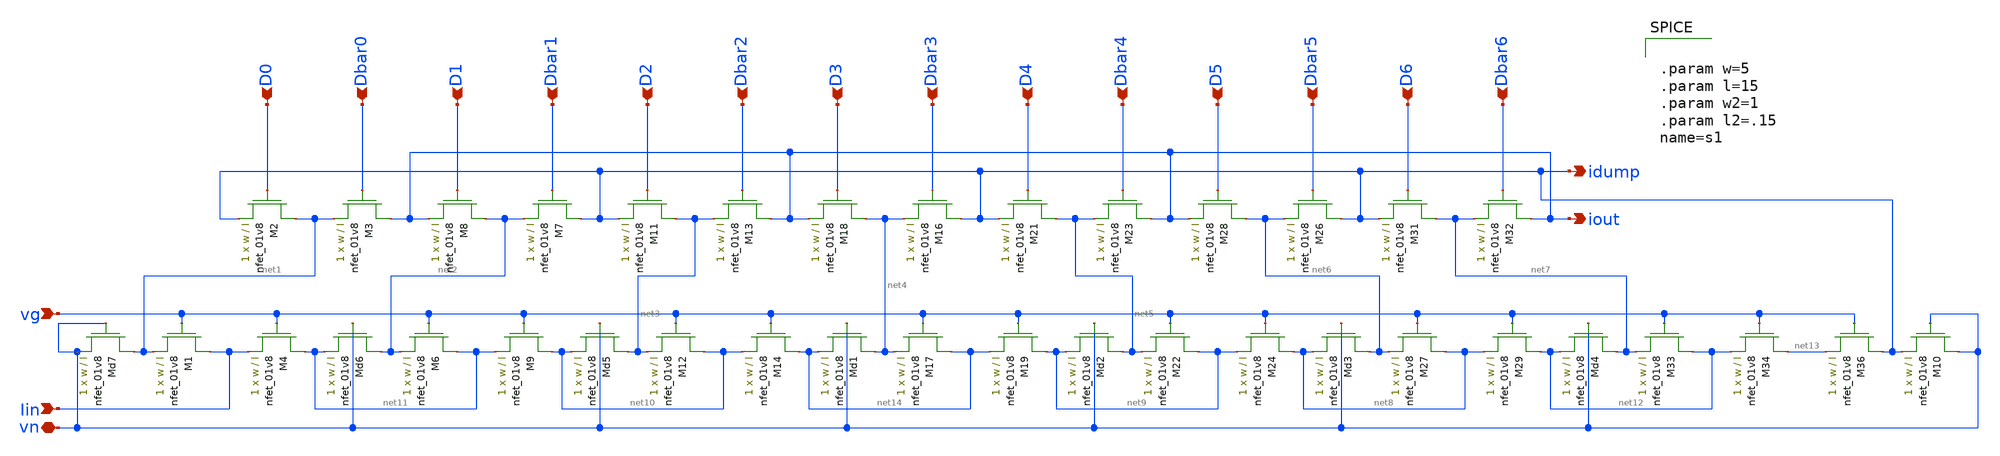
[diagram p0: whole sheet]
** sch_path: schematic/ladder_LDS.sch
**.subckt ladder_LDS iout idump vn vg D0 Dbar0 D1 D2 D3 D4 D5 D6 Dbar1 Dbar2 Dbar3 Dbar4 Dbar5 Dbar6
*+ Iin
*.opin iout
*.opin idump
*.iopin vn
*.ipin vg
*.ipin D0
*.ipin Dbar0
*.ipin D1
*.ipin D2
*.ipin D3
*.ipin D4
*.ipin D5
*.ipin D6
*.ipin Dbar1
*.ipin Dbar2
*.ipin Dbar3
*.ipin Dbar4
*.ipin Dbar5
*.ipin Dbar6
*.ipin Iin
XM1 Iin vg net1 GND sky130_fd_pr__nfet_01v8 L=l W=w nf=1 ad='int((nf+1)/2) * W/nf * 0.29' as='int((nf+2)/2) * W/nf * 0.29'
+ pd='2*int((nf+1)/2) * (W/nf + 0.29)' ps='2*int((nf+2)/2) * (W/nf + 0.29)' nrd='0.29 / W' nrs='0.29 / W'
+ sa=0 sb=0 sd=0 mult=1 m=1
XM2 net1 D0 idump GND sky130_fd_pr__nfet_01v8 L=l W=w nf=1 ad='int((nf+1)/2) * W/nf * 0.29' as='int((nf+2)/2) * W/nf * 0.29'
+ pd='2*int((nf+1)/2) * (W/nf + 0.29)' ps='2*int((nf+2)/2) * (W/nf + 0.29)' nrd='0.29 / W' nrs='0.29 / W'
+ sa=0 sb=0 sd=0 mult=1 m=1
XM3 iout Dbar0 net1 GND sky130_fd_pr__nfet_01v8 L=l W=w nf=1 ad='int((nf+1)/2) * W/nf * 0.29' as='int((nf+2)/2) * W/nf * 0.29'
+ pd='2*int((nf+1)/2) * (W/nf + 0.29)' ps='2*int((nf+2)/2) * (W/nf + 0.29)' nrd='0.29 / W' nrs='0.29 / W'
+ sa=0 sb=0 sd=0 mult=1 m=1
XM4 net11 vg Iin GND sky130_fd_pr__nfet_01v8 L=l W=w nf=1 ad='int((nf+1)/2) * W/nf * 0.29' as='int((nf+2)/2) * W/nf * 0.29'
+ pd='2*int((nf+1)/2) * (W/nf + 0.29)' ps='2*int((nf+2)/2) * (W/nf + 0.29)' nrd='0.29 / W' nrs='0.29 / W'
+ sa=0 sb=0 sd=0 mult=1 m=1
XM6 net11 vg net2 GND sky130_fd_pr__nfet_01v8 L=l W=w nf=1 ad='int((nf+1)/2) * W/nf * 0.29' as='int((nf+2)/2) * W/nf * 0.29'
+ pd='2*int((nf+1)/2) * (W/nf + 0.29)' ps='2*int((nf+2)/2) * (W/nf + 0.29)' nrd='0.29 / W' nrs='0.29 / W'
+ sa=0 sb=0 sd=0 mult=1 m=1
XM7 idump Dbar1 net2 GND sky130_fd_pr__nfet_01v8 L=l W=w nf=1 ad='int((nf+1)/2) * W/nf * 0.29' as='int((nf+2)/2) * W/nf * 0.29'
+ pd='2*int((nf+1)/2) * (W/nf + 0.29)' ps='2*int((nf+2)/2) * (W/nf + 0.29)' nrd='0.29 / W' nrs='0.29 / W'
+ sa=0 sb=0 sd=0 mult=1 m=1
XM8 net2 D1 iout GND sky130_fd_pr__nfet_01v8 L=l W=w nf=1 ad='int((nf+1)/2) * W/nf * 0.29' as='int((nf+2)/2) * W/nf * 0.29'
+ pd='2*int((nf+1)/2) * (W/nf + 0.29)' ps='2*int((nf+2)/2) * (W/nf + 0.29)' nrd='0.29 / W' nrs='0.29 / W'
+ sa=0 sb=0 sd=0 mult=1 m=1
XM9 net10 vg net11 GND sky130_fd_pr__nfet_01v8 L=l W=w nf=1 ad='int((nf+1)/2) * W/nf * 0.29' as='int((nf+2)/2) * W/nf * 0.29'
+ pd='2*int((nf+1)/2) * (W/nf + 0.29)' ps='2*int((nf+2)/2) * (W/nf + 0.29)' nrd='0.29 / W' nrs='0.29 / W'
+ sa=0 sb=0 sd=0 mult=1 m=1
XM11 net3 D2 idump GND sky130_fd_pr__nfet_01v8 L=l W=w nf=1 ad='int((nf+1)/2) * W/nf * 0.29' as='int((nf+2)/2) * W/nf * 0.29'
+ pd='2*int((nf+1)/2) * (W/nf + 0.29)' ps='2*int((nf+2)/2) * (W/nf + 0.29)' nrd='0.29 / W' nrs='0.29 / W'
+ sa=0 sb=0 sd=0 mult=1 m=1
XM12 net10 vg net3 GND sky130_fd_pr__nfet_01v8 L=l W=w nf=1 ad='int((nf+1)/2) * W/nf * 0.29' as='int((nf+2)/2) * W/nf * 0.29'
+ pd='2*int((nf+1)/2) * (W/nf + 0.29)' ps='2*int((nf+2)/2) * (W/nf + 0.29)' nrd='0.29 / W' nrs='0.29 / W'
+ sa=0 sb=0 sd=0 mult=1 m=1
XM13 iout Dbar2 net3 GND sky130_fd_pr__nfet_01v8 L=l W=w nf=1 ad='int((nf+1)/2) * W/nf * 0.29' as='int((nf+2)/2) * W/nf * 0.29'
+ pd='2*int((nf+1)/2) * (W/nf + 0.29)' ps='2*int((nf+2)/2) * (W/nf + 0.29)' nrd='0.29 / W' nrs='0.29 / W'
+ sa=0 sb=0 sd=0 mult=1 m=1
XM14 net14 vg net10 GND sky130_fd_pr__nfet_01v8 L=l W=w nf=1 ad='int((nf+1)/2) * W/nf * 0.29' as='int((nf+2)/2) * W/nf * 0.29'
+ pd='2*int((nf+1)/2) * (W/nf + 0.29)' ps='2*int((nf+2)/2) * (W/nf + 0.29)' nrd='0.29 / W' nrs='0.29 / W'
+ sa=0 sb=0 sd=0 mult=1 m=1
XM16 idump Dbar3 net4 GND sky130_fd_pr__nfet_01v8 L=l W=w nf=1 ad='int((nf+1)/2) * W/nf * 0.29' as='int((nf+2)/2) * W/nf * 0.29'
+ pd='2*int((nf+1)/2) * (W/nf + 0.29)' ps='2*int((nf+2)/2) * (W/nf + 0.29)' nrd='0.29 / W' nrs='0.29 / W'
+ sa=0 sb=0 sd=0 mult=1 m=1
XM17 net14 vg net4 GND sky130_fd_pr__nfet_01v8 L=l W=w nf=1 ad='int((nf+1)/2) * W/nf * 0.29' as='int((nf+2)/2) * W/nf * 0.29'
+ pd='2*int((nf+1)/2) * (W/nf + 0.29)' ps='2*int((nf+2)/2) * (W/nf + 0.29)' nrd='0.29 / W' nrs='0.29 / W'
+ sa=0 sb=0 sd=0 mult=1 m=1
XM18 net4 D3 iout GND sky130_fd_pr__nfet_01v8 L=l W=w nf=1 ad='int((nf+1)/2) * W/nf * 0.29' as='int((nf+2)/2) * W/nf * 0.29'
+ pd='2*int((nf+1)/2) * (W/nf + 0.29)' ps='2*int((nf+2)/2) * (W/nf + 0.29)' nrd='0.29 / W' nrs='0.29 / W'
+ sa=0 sb=0 sd=0 mult=1 m=1
XM19 net9 vg net14 GND sky130_fd_pr__nfet_01v8 L=l W=w nf=1 ad='int((nf+1)/2) * W/nf * 0.29' as='int((nf+2)/2) * W/nf * 0.29'
+ pd='2*int((nf+1)/2) * (W/nf + 0.29)' ps='2*int((nf+2)/2) * (W/nf + 0.29)' nrd='0.29 / W' nrs='0.29 / W'
+ sa=0 sb=0 sd=0 mult=1 m=1
XM21 net5 D4 idump GND sky130_fd_pr__nfet_01v8 L=l W=w nf=1 ad='int((nf+1)/2) * W/nf * 0.29' as='int((nf+2)/2) * W/nf * 0.29'
+ pd='2*int((nf+1)/2) * (W/nf + 0.29)' ps='2*int((nf+2)/2) * (W/nf + 0.29)' nrd='0.29 / W' nrs='0.29 / W'
+ sa=0 sb=0 sd=0 mult=1 m=1
XM22 net9 vg net5 GND sky130_fd_pr__nfet_01v8 L=l W=w nf=1 ad='int((nf+1)/2) * W/nf * 0.29' as='int((nf+2)/2) * W/nf * 0.29'
+ pd='2*int((nf+1)/2) * (W/nf + 0.29)' ps='2*int((nf+2)/2) * (W/nf + 0.29)' nrd='0.29 / W' nrs='0.29 / W'
+ sa=0 sb=0 sd=0 mult=1 m=1
XM23 iout Dbar4 net5 GND sky130_fd_pr__nfet_01v8 L=l W=w nf=1 ad='int((nf+1)/2) * W/nf * 0.29' as='int((nf+2)/2) * W/nf * 0.29'
+ pd='2*int((nf+1)/2) * (W/nf + 0.29)' ps='2*int((nf+2)/2) * (W/nf + 0.29)' nrd='0.29 / W' nrs='0.29 / W'
+ sa=0 sb=0 sd=0 mult=1 m=1
XM24 net8 vg net9 GND sky130_fd_pr__nfet_01v8 L=l W=w nf=1 ad='int((nf+1)/2) * W/nf * 0.29' as='int((nf+2)/2) * W/nf * 0.29'
+ pd='2*int((nf+1)/2) * (W/nf + 0.29)' ps='2*int((nf+2)/2) * (W/nf + 0.29)' nrd='0.29 / W' nrs='0.29 / W'
+ sa=0 sb=0 sd=0 mult=1 m=1
XM26 idump Dbar5 net6 GND sky130_fd_pr__nfet_01v8 L=l W=w nf=1 ad='int((nf+1)/2) * W/nf * 0.29' as='int((nf+2)/2) * W/nf * 0.29'
+ pd='2*int((nf+1)/2) * (W/nf + 0.29)' ps='2*int((nf+2)/2) * (W/nf + 0.29)' nrd='0.29 / W' nrs='0.29 / W'
+ sa=0 sb=0 sd=0 mult=1 m=1
XM27 net8 vg net6 GND sky130_fd_pr__nfet_01v8 L=l W=w nf=1 ad='int((nf+1)/2) * W/nf * 0.29' as='int((nf+2)/2) * W/nf * 0.29'
+ pd='2*int((nf+1)/2) * (W/nf + 0.29)' ps='2*int((nf+2)/2) * (W/nf + 0.29)' nrd='0.29 / W' nrs='0.29 / W'
+ sa=0 sb=0 sd=0 mult=1 m=1
XM28 net6 D5 iout GND sky130_fd_pr__nfet_01v8 L=l W=w nf=1 ad='int((nf+1)/2) * W/nf * 0.29' as='int((nf+2)/2) * W/nf * 0.29'
+ pd='2*int((nf+1)/2) * (W/nf + 0.29)' ps='2*int((nf+2)/2) * (W/nf + 0.29)' nrd='0.29 / W' nrs='0.29 / W'
+ sa=0 sb=0 sd=0 mult=1 m=1
XM29 net12 vg net8 GND sky130_fd_pr__nfet_01v8 L=l W=w nf=1 ad='int((nf+1)/2) * W/nf * 0.29' as='int((nf+2)/2) * W/nf * 0.29'
+ pd='2*int((nf+1)/2) * (W/nf + 0.29)' ps='2*int((nf+2)/2) * (W/nf + 0.29)' nrd='0.29 / W' nrs='0.29 / W'
+ sa=0 sb=0 sd=0 mult=1 m=1
XM31 net7 D6 idump GND sky130_fd_pr__nfet_01v8 L=l W=w nf=1 ad='int((nf+1)/2) * W/nf * 0.29' as='int((nf+2)/2) * W/nf * 0.29'
+ pd='2*int((nf+1)/2) * (W/nf + 0.29)' ps='2*int((nf+2)/2) * (W/nf + 0.29)' nrd='0.29 / W' nrs='0.29 / W'
+ sa=0 sb=0 sd=0 mult=1 m=1
XM32 iout Dbar6 net7 GND sky130_fd_pr__nfet_01v8 L=l W=w nf=1 ad='int((nf+1)/2) * W/nf * 0.29' as='int((nf+2)/2) * W/nf * 0.29'
+ pd='2*int((nf+1)/2) * (W/nf + 0.29)' ps='2*int((nf+2)/2) * (W/nf + 0.29)' nrd='0.29 / W' nrs='0.29 / W'
+ sa=0 sb=0 sd=0 mult=1 m=1
XM33 net12 vg net7 GND sky130_fd_pr__nfet_01v8 L=l W=w nf=1 ad='int((nf+1)/2) * W/nf * 0.29' as='int((nf+2)/2) * W/nf * 0.29'
+ pd='2*int((nf+1)/2) * (W/nf + 0.29)' ps='2*int((nf+2)/2) * (W/nf + 0.29)' nrd='0.29 / W' nrs='0.29 / W'
+ sa=0 sb=0 sd=0 mult=1 m=1
XM34 net13 vg net12 GND sky130_fd_pr__nfet_01v8 L=l W=w nf=1 ad='int((nf+1)/2) * W/nf * 0.29' as='int((nf+2)/2) * W/nf * 0.29'
+ pd='2*int((nf+1)/2) * (W/nf + 0.29)' ps='2*int((nf+2)/2) * (W/nf + 0.29)' nrd='0.29 / W' nrs='0.29 / W'
+ sa=0 sb=0 sd=0 mult=1 m=1
XM36 idump vg net13 GND sky130_fd_pr__nfet_01v8 L=l W=w nf=1 ad='int((nf+1)/2) * W/nf * 0.29' as='int((nf+2)/2) * W/nf * 0.29'
+ pd='2*int((nf+1)/2) * (W/nf + 0.29)' ps='2*int((nf+2)/2) * (W/nf + 0.29)' nrd='0.29 / W' nrs='0.29 / W'
+ sa=0 sb=0 sd=0 mult=1 m=1
XMd1 net4 vn net14 GND sky130_fd_pr__nfet_01v8 L=l W=w nf=1 ad='int((nf+1)/2) * W/nf * 0.29' as='int((nf+2)/2) * W/nf * 0.29'
+ pd='2*int((nf+1)/2) * (W/nf + 0.29)' ps='2*int((nf+2)/2) * (W/nf + 0.29)' nrd='0.29 / W' nrs='0.29 / W'
+ sa=0 sb=0 sd=0 mult=1 m=1
XMd2 net5 vn net9 GND sky130_fd_pr__nfet_01v8 L=l W=w nf=1 ad='int((nf+1)/2) * W/nf * 0.29' as='int((nf+2)/2) * W/nf * 0.29'
+ pd='2*int((nf+1)/2) * (W/nf + 0.29)' ps='2*int((nf+2)/2) * (W/nf + 0.29)' nrd='0.29 / W' nrs='0.29 / W'
+ sa=0 sb=0 sd=0 mult=1 m=1
XMd3 net6 vn net8 GND sky130_fd_pr__nfet_01v8 L=l W=w nf=1 ad='int((nf+1)/2) * W/nf * 0.29' as='int((nf+2)/2) * W/nf * 0.29'
+ pd='2*int((nf+1)/2) * (W/nf + 0.29)' ps='2*int((nf+2)/2) * (W/nf + 0.29)' nrd='0.29 / W' nrs='0.29 / W'
+ sa=0 sb=0 sd=0 mult=1 m=1
XMd4 net7 vn net12 GND sky130_fd_pr__nfet_01v8 L=l W=w nf=1 ad='int((nf+1)/2) * W/nf * 0.29' as='int((nf+2)/2) * W/nf * 0.29'
+ pd='2*int((nf+1)/2) * (W/nf + 0.29)' ps='2*int((nf+2)/2) * (W/nf + 0.29)' nrd='0.29 / W' nrs='0.29 / W'
+ sa=0 sb=0 sd=0 mult=1 m=1
XMd5 net3 vn net10 GND sky130_fd_pr__nfet_01v8 L=l W=w nf=1 ad='int((nf+1)/2) * W/nf * 0.29' as='int((nf+2)/2) * W/nf * 0.29'
+ pd='2*int((nf+1)/2) * (W/nf + 0.29)' ps='2*int((nf+2)/2) * (W/nf + 0.29)' nrd='0.29 / W' nrs='0.29 / W'
+ sa=0 sb=0 sd=0 mult=1 m=1
XMd6 net2 vn net11 GND sky130_fd_pr__nfet_01v8 L=l W=w nf=1 ad='int((nf+1)/2) * W/nf * 0.29' as='int((nf+2)/2) * W/nf * 0.29'
+ pd='2*int((nf+1)/2) * (W/nf + 0.29)' ps='2*int((nf+2)/2) * (W/nf + 0.29)' nrd='0.29 / W' nrs='0.29 / W'
+ sa=0 sb=0 sd=0 mult=1 m=1
XMd7 net1 vn vn GND sky130_fd_pr__nfet_01v8 L=l W=w nf=1 ad='int((nf+1)/2) * W/nf * 0.29' as='int((nf+2)/2) * W/nf * 0.29'
+ pd='2*int((nf+1)/2) * (W/nf + 0.29)' ps='2*int((nf+2)/2) * (W/nf + 0.29)' nrd='0.29 / W' nrs='0.29 / W'
+ sa=0 sb=0 sd=0 mult=1 m=1
XM10 vn vn idump GND sky130_fd_pr__nfet_01v8 L=l W=w nf=1 ad='int((nf+1)/2) * W/nf * 0.29' as='int((nf+2)/2) * W/nf * 0.29'
+ pd='2*int((nf+1)/2) * (W/nf + 0.29)' ps='2*int((nf+2)/2) * (W/nf + 0.29)' nrd='0.29 / W' nrs='0.29 / W'
+ sa=0 sb=0 sd=0 mult=1 m=1
**** begin user architecture code


.param w=5
.param l=15
.param w2=1
.param l2=.15
name=s1

**** end user architecture code
**.ends
.end
